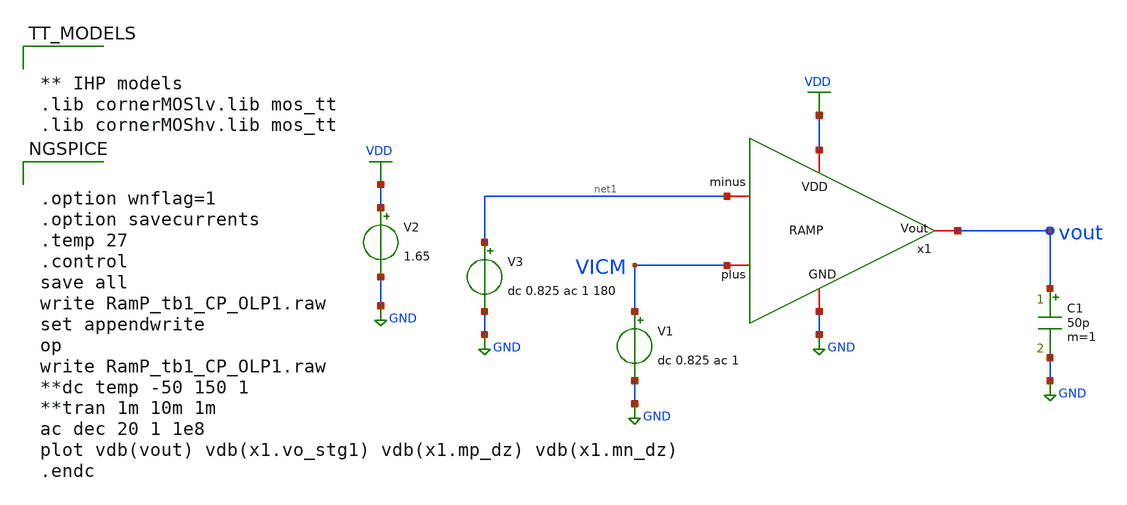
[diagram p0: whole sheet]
** sch_path: Design Files/RAMP/RAMP-Test/RamP_tb1_CP_OLP1.sch
**.subckt RamP_tb1_CP_OLP1
x1 VDD VICM vout net1 GND RAMP
V1 VICM GND dc 0.825 ac 1
V2 VDD GND 1.65
C1 vout GND 50p m=1
V3 net1 GND dc 0.825 ac 1 180
**** begin user architecture code


** IHP models
.lib cornerMOSlv.lib mos_tt
.lib cornerMOShv.lib mos_tt




.option wnflag=1
.option savecurrents
.temp 27
.control
save all
write RamP_tb1_CP_OLP1.raw
set appendwrite
op
write RamP_tb1_CP_OLP1.raw
**dc temp -50 150 1
**tran 1m 10m 1m
ac dec 20 1 1e8
plot vdb(vout) vdb(x1.vo_stg1) vdb(x1.mp_dz) vdb(x1.mn_dz)
.endc


**** end user architecture code
**.ends

* expanding   symbol:  /foss/designs/RAMP/Fully-Diff-RAMP/RAMP.sym # of pins=5
** sym_path: Design Files/RAMP/Fully-Diff-RAMP/RAMP.sym
** sch_path: Design Files/RAMP/Fully-Diff-RAMP/RAMP.sch
.subckt RAMP VDD minus Vout plus GND
*.iopin GND
*.iopin plus
*.iopin minus
*.iopin Vout
*.iopin VDD
x1 VDD Vo_STG1 V1_CM plus minus GND STG1
x2 VDD net2 mp_dz Vo_STG1 mn_dz net1 GND STG2
XM1 Vout mn_dz GND GND sg13_hv_nmos w=2.3u l=1u ng=1 m=4 mm_ok=1
XM2 Vout mp_dz VDD VDD sg13_hv_pmos w=4.5u l=0.5u ng=1 m=4 mm_ok=1
x3 VDD net2 V1_CM net1 GND STG2_Replica
x4 VDD V1_CM GND STG1-CM
.ends


* expanding   symbol:  /foss/designs/RAMP/Fully-Diff-RAMP/STG1.sym # of pins=6
** sym_path: Design Files/RAMP/Fully-Diff-RAMP/STG1.sym
** sch_path: Design Files/RAMP/Fully-Diff-RAMP/STG1.sch
.subckt STG1 VDD Vo1 V1_CM Vin Vip GND
*.iopin VDD
*.iopin GND
*.opin Vo1
*.ipin Vip
*.ipin Vin
*.ipin V1_CM
R1 net3 net2 100k m=1
R3 net3 Vo1 100k m=1
XMN_STG1_IP_N1 net2 Vip net4 GND sg13_lv_nmos w=1.563u l=0.5u ng=1 m=2 mm_ok=1
XMN_STG1_IP_N2 Vo1 Vin net4 GND sg13_lv_nmos w=1.563u l=0.5u ng=1 m=2 mm_ok=1
I0 net4 GND 10u
XMP_STG1_CL_P1 net2 net1 VDD VDD sg13_hv_pmos w=0.5u l=1u ng=1 m=1 mm_ok=1
XMP_STG1_CL_P2 Vo1 net1 VDD VDD sg13_hv_pmos w=0.5u l=1u ng=1 m=1 mm_ok=1
E1 net1 GND net3 V1_CM 10k
.ends


* expanding   symbol:  /foss/designs/RAMP/Fully-Diff-RAMP/STG2.sym # of pins=7
** sym_path: Design Files/RAMP/Fully-Diff-RAMP/STG2.sym
** sch_path: Design Files/RAMP/Fully-Diff-RAMP/STG2.sch
.subckt STG2 VDD VCTRL_P VDZP Vin_2 VDZN VCTRL_N GND
*.ipin Vin_2
*.ipin VDD
*.ipin GND
*.ipin VCTRL_P
*.ipin VCTRL_N
*.opin VDZN
*.opin VDZP
XMN_STG2_3N1 VDZN Vin_2 GND GND sg13_lv_nmos w=0.15u l=0.13u ng=1 m=1 mm_ok=1
XMN_STG2_3P1 VDZN Vin_2 net1 VDD sg13_lv_pmos w=0.15u l=0.13u ng=1 m=3 mm_ok=1
XMP_DZ_STG2_3N net1 VCTRL_P VDD VDD sg13_lv_pmos w=0.15u l=0.13u ng=1 m=5 mm_ok=1
XMP_STG2_3P2 VDZP Vin_2 net2 net2 sg13_lv_nmos w=0.15u l=0.13u ng=1 m=1 mm_ok=1
XMP_STG2_3P1 VDZP Vin_2 VDD VDD sg13_lv_pmos w=0.15u l=0.13u ng=1 m=1 mm_ok=1
XMN_DZ_STG2_3P net2 VCTRL_N GND GND sg13_lv_nmos w=0.15u l=0.13u ng=1 m=1 mm_ok=1
.ends


* expanding   symbol:  /foss/designs/RAMP/Fully-Diff-RAMP/STG2_Replica.sym # of pins=5
** sym_path: Design Files/RAMP/Fully-Diff-RAMP/STG2_Replica.sym
** sch_path: Design Files/RAMP/Fully-Diff-RAMP/STG2_Replica.sch
.subckt STG2_Replica VDD VCTRLP Vin_STG2 VCTRLN GND
*.ipin Vin_STG2
*.iopin VDD
*.iopin GND
*.opin VCTRLP
*.opin VCTRLN
XMN_STG2_3N1 net1 Vin_STG2 GND GND sg13_lv_nmos w=0.15u l=0.13u ng=1 m=1 mm_ok=1
XMN_STG2_3P1 net1 Vin_STG2 net2 VDD sg13_lv_pmos w=0.15u l=0.13u ng=1 m=3 mm_ok=1
XMP_DZ_STG2_3N net2 VCTRLP VDD VDD sg13_lv_pmos w=0.15u l=0.13u ng=1 m=5 mm_ok=1
XMP_STG2_3P2 net4 Vin_STG2 net3 net3 sg13_lv_nmos w=0.15u l=0.13u ng=1 m=1 mm_ok=1
XMP_STG2_3P1 net4 Vin_STG2 VDD VDD sg13_lv_pmos w=0.15u l=0.13u ng=1 m=1 mm_ok=1
XMN_DZ_STG2_3P net3 VCTRLN GND GND sg13_lv_nmos w=0.15u l=0.13u ng=1 m=1 mm_ok=1
XMN_STG2_3N_R net5 net5 GND GND sg13_hv_nmos w=2.3u l=1u ng=1 m=1 mm_ok=1
I0 VDD net5 1u
x1 VDD net1 net5 VCTRLP GND POTA
XMP_STG2_3P_R net6 net6 VDD VDD sg13_hv_pmos w=4.5u l=0.5u ng=1 m=1 mm_ok=1
I1 net6 GND 1u
x2 VDD VCTRLN net4 net6 GND NOTA
.ends


* expanding   symbol:  /foss/designs/RAMP/Fully-Diff-RAMP/STG1-CM.sym # of pins=3
** sym_path: Design Files/RAMP/Fully-Diff-RAMP/STG1-CM.sym
** sch_path: Design Files/RAMP/Fully-Diff-RAMP/STG1-CM.sch
.subckt STG1-CM VDD V_CM1 GND
*.ipin VDD
*.ipin GND
*.opin V_CM1
XM9 V_CM1 V_CM1 GND GND sg13_lv_nmos w=0.15u l=0.13u ng=1 m=1 mm_ok=1
XM10 V_CM1 V_CM1 net1 VDD sg13_lv_pmos w=0.15u l=0.13u ng=1 m=3 mm_ok=1
XM11 net1 GND VDD VDD sg13_lv_pmos w=0.15u l=0.13u ng=1 m=5 mm_ok=1
XM12 V_CM1 V_CM1 net2 net2 sg13_lv_nmos w=0.15u l=0.13u ng=1 m=1 mm_ok=1
XM13 V_CM1 V_CM1 VDD VDD sg13_lv_pmos w=0.15u l=0.13u ng=1 m=1 mm_ok=1
XM14 net2 VDD GND GND sg13_lv_nmos w=0.15u l=0.13u ng=1 m=1 mm_ok=1
.ends


* expanding   symbol:  /foss/designs/RAMP/OTA/POTA.sym # of pins=5
** sym_path: Design Files/RAMP/OTA/POTA.sym
** sch_path: Design Files/RAMP/OTA/POTA.sch
.subckt POTA VDD PLUS MINUS Vout GND
*.ipin VDD
*.ipin GND
*.ipin PLUS
*.ipin MINUS
*.opin Vout
XM2 net2 PLUS net1 VDD sg13_lv_pmos w=1.2u l=0.5u ng=1 m=2 mm_ok=1
XM3 Vout MINUS net1 VDD sg13_lv_pmos w=1.2u l=0.5u ng=1 m=2 mm_ok=1
XM4 Vout net2 GND GND sg13_hv_nmos w=0.5u l=2u ng=1 m=1 mm_ok=1
XM5 net2 net2 GND GND sg13_hv_nmos w=0.5u l=2u ng=1 m=1 mm_ok=1
I1 VDD net1 2u
.ends


* expanding   symbol:  /foss/designs/RAMP/OTA/NOTA.sym # of pins=5
** sym_path: Design Files/RAMP/OTA/NOTA.sym
** sch_path: Design Files/RAMP/OTA/NOTA.sch
.subckt NOTA VDD Vout PLUS MINUS GND
*.ipin VDD
*.ipin GND
*.ipin PLUS
*.ipin MINUS
*.opin Vout
XM1 net2 PLUS net1 GND sg13_hv_nmos w=1.75u l=1u ng=1 m=2 mm_ok=1
XM2 Vout MINUS net1 GND sg13_hv_nmos w=1.75u l=1u ng=1 m=2 mm_ok=1
I0 net1 GND 2u
XM3 Vout net2 VDD VDD sg13_hv_pmos w=0.5u l=0.75u ng=1 m=1 mm_ok=1
XM4 net2 net2 VDD VDD sg13_hv_pmos w=0.5u l=0.75u ng=1 m=1 mm_ok=1
.ends

.GLOBAL VDD
.GLOBAL GND
.end
